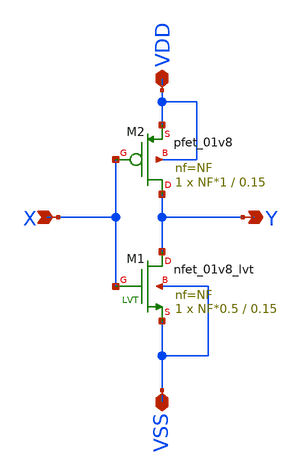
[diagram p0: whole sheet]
** sch_path: xschem_lib/DFFRAM_full_custom/inv.sch
**.subckt inv VSS X Y VDD
*.iopin VSS
*.ipin X
*.opin Y
*.iopin VDD
XM1 Y X VSS VSS sky130_fd_pr__nfet_01v8_lvt L=0.15 W=NF*0.5 nf=NF ad='int((nf+1)/2) * W/nf * 0.29' as='int((nf+2)/2) * W/nf * 0.29'
+ pd='2*int((nf+1)/2) * (W/nf + 0.29)' ps='2*int((nf+2)/2) * (W/nf + 0.29)' nrd='0.29 / W' nrs='0.29 / W'
+ sa=0 sb=0 sd=0 mult=1 m=1
XM2 Y X VDD VDD sky130_fd_pr__pfet_01v8 L=0.15 W=NF*1 nf=NF ad='int((nf+1)/2) * W/nf * 0.29' as='int((nf+2)/2) * W/nf * 0.29'
+ pd='2*int((nf+1)/2) * (W/nf + 0.29)' ps='2*int((nf+2)/2) * (W/nf + 0.29)' nrd='0.29 / W' nrs='0.29 / W'
+ sa=0 sb=0 sd=0 mult=1 m=1
**.ends
.end
